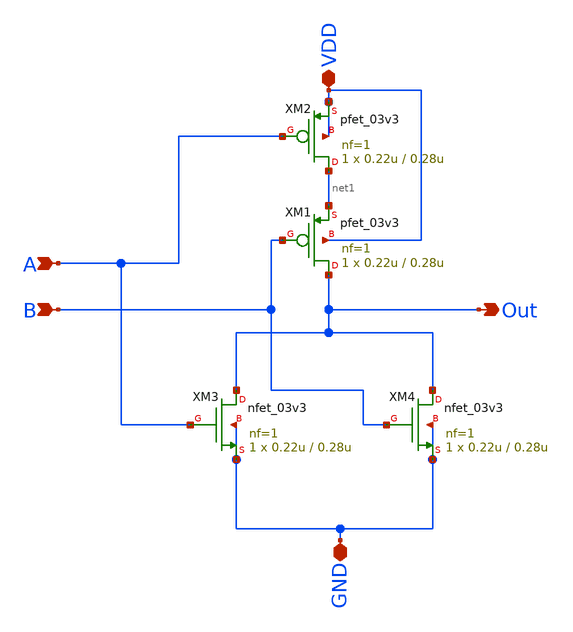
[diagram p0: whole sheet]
** sch_path: 2bit_Comparator/2x_drive/my_nor.sch
**.subckt my_nor A B VDD GND Out
*.ipin A
*.ipin B
*.iopin VDD
*.iopin GND
*.opin Out
XM2 net1 A VDD VDD pfet_03v3 L=0.28u W=0.22u nf=1 ad='int((nf+1)/2) * W/nf * 0.18u' as='int((nf+2)/2) * W/nf * 0.18u'
+ pd='2*int((nf+1)/2) * (W/nf + 0.18u)' ps='2*int((nf+2)/2) * (W/nf + 0.18u)' nrd='0.18u / W' nrs='0.18u / W'
+ sa=0 sb=0 sd=0 m=1
XM1 Out B net1 VDD pfet_03v3 L=0.28u W=0.22u nf=1 ad='int((nf+1)/2) * W/nf * 0.18u' as='int((nf+2)/2) * W/nf * 0.18u'
+ pd='2*int((nf+1)/2) * (W/nf + 0.18u)' ps='2*int((nf+2)/2) * (W/nf + 0.18u)' nrd='0.18u / W' nrs='0.18u / W'
+ sa=0 sb=0 sd=0 m=1
XM3 Out A GND GND nfet_03v3 L=0.28u W=0.22u nf=1 ad='int((nf+1)/2) * W/nf * 0.18u' as='int((nf+2)/2) * W/nf * 0.18u'
+ pd='2*int((nf+1)/2) * (W/nf + 0.18u)' ps='2*int((nf+2)/2) * (W/nf + 0.18u)' nrd='0.18u / W' nrs='0.18u / W'
+ sa=0 sb=0 sd=0 m=1
XM4 Out B GND GND nfet_03v3 L=0.28u W=0.22u nf=1 ad='int((nf+1)/2) * W/nf * 0.18u' as='int((nf+2)/2) * W/nf * 0.18u'
+ pd='2*int((nf+1)/2) * (W/nf + 0.18u)' ps='2*int((nf+2)/2) * (W/nf + 0.18u)' nrd='0.18u / W' nrs='0.18u / W'
+ sa=0 sb=0 sd=0 m=1
**.ends
.end
